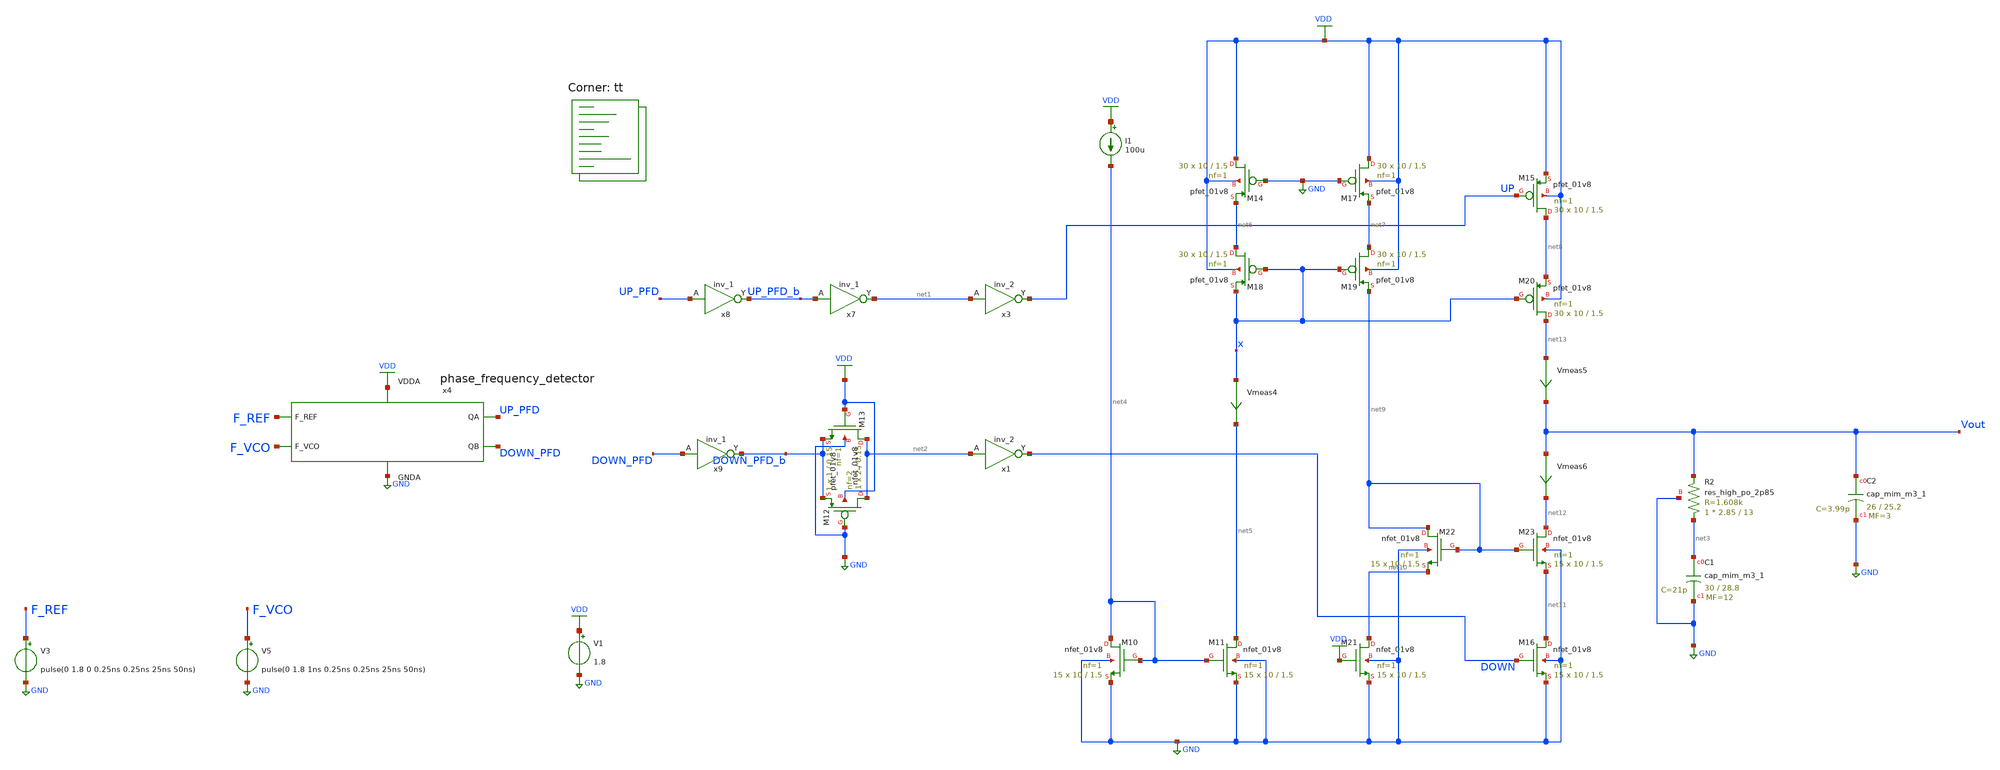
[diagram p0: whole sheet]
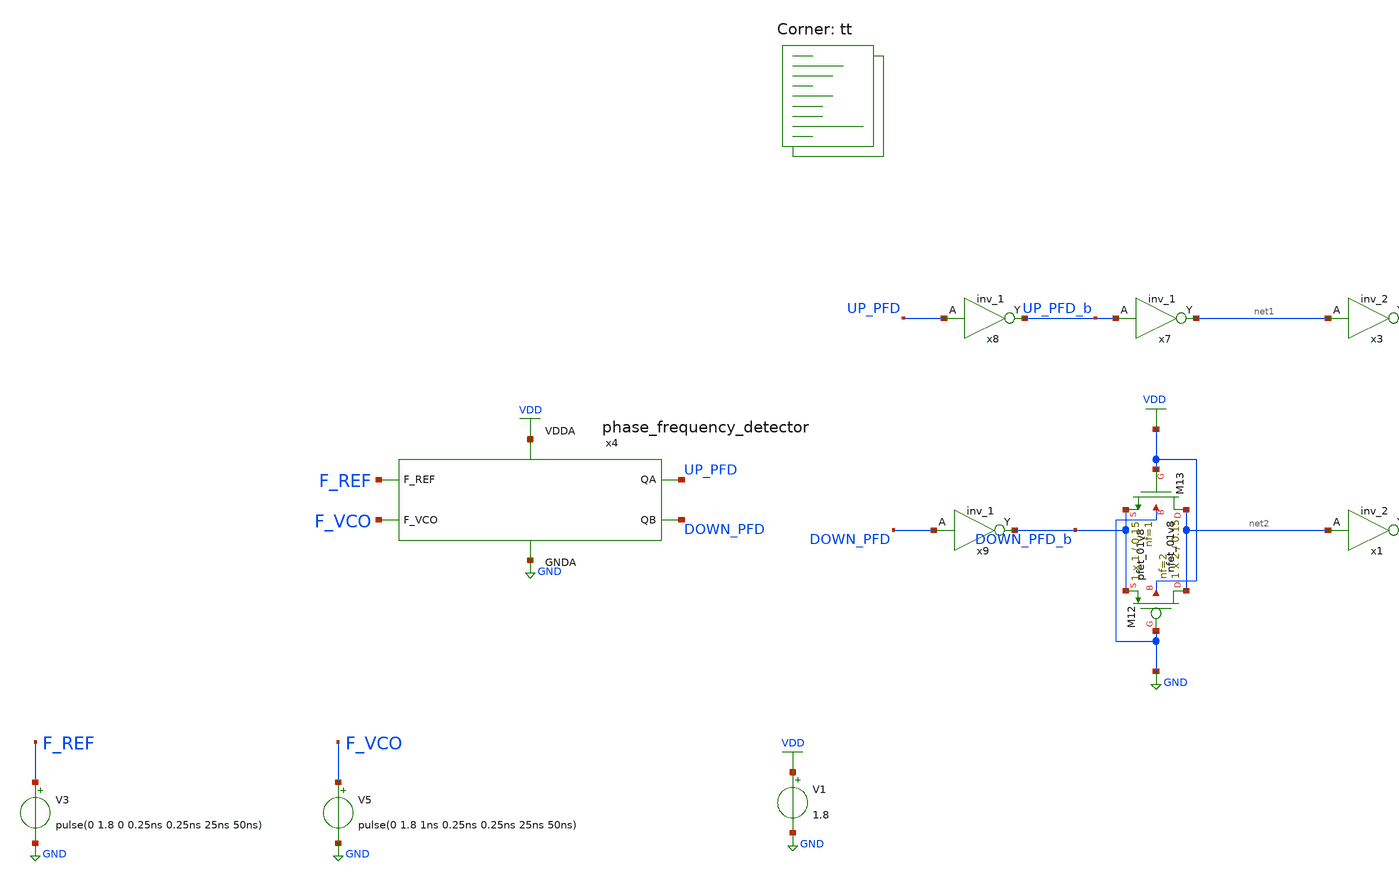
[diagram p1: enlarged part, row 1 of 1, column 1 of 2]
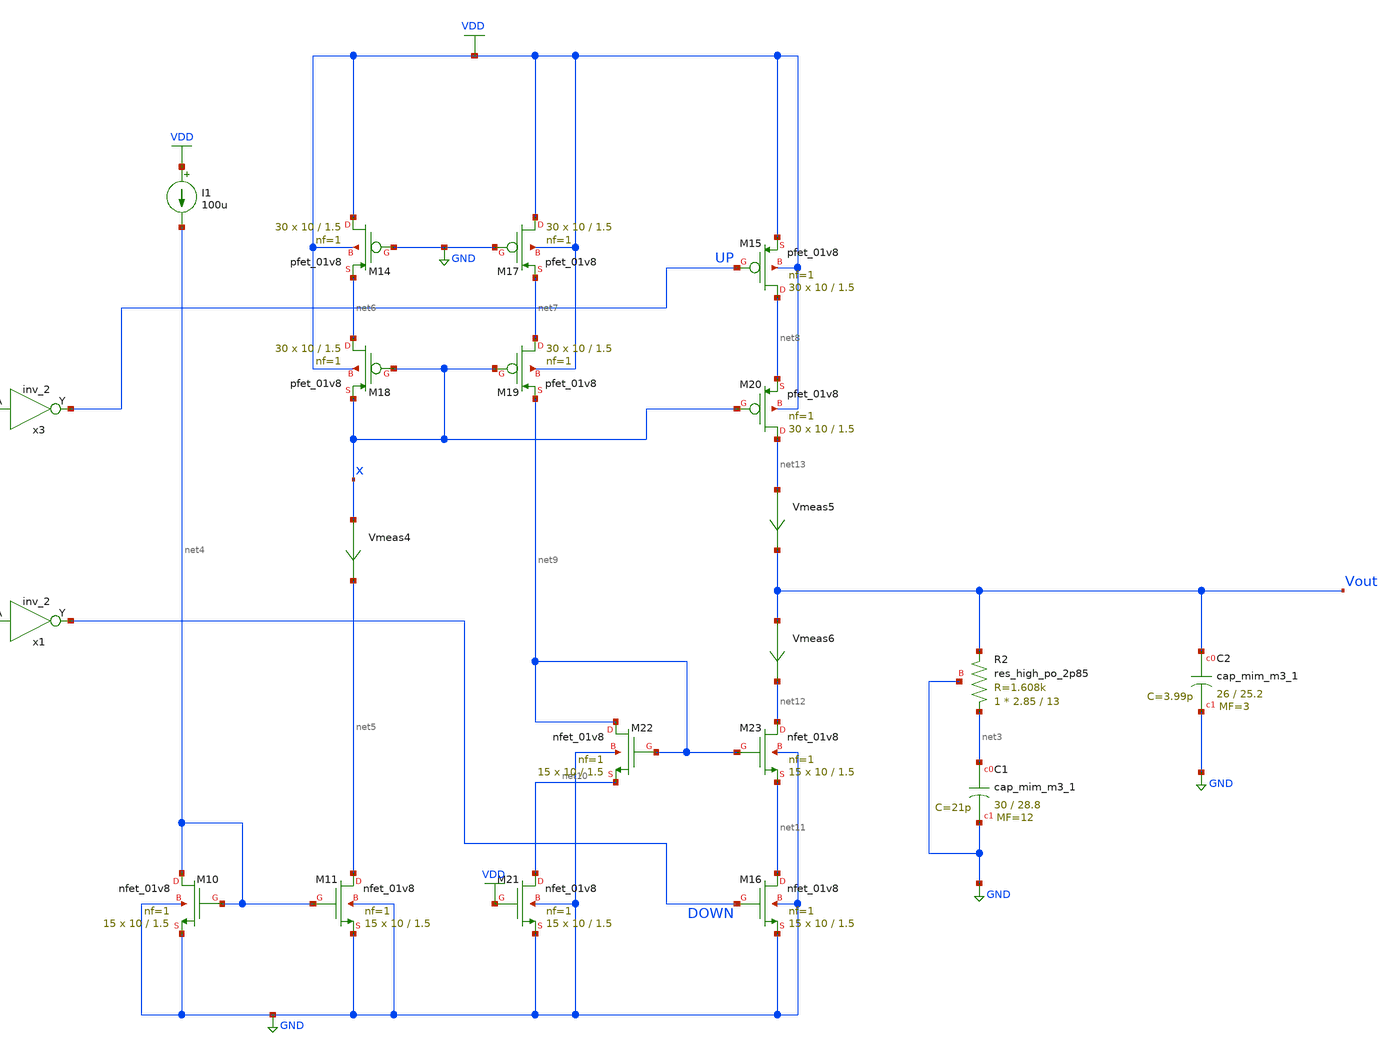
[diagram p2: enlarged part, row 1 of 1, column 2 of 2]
** sch_path: projects/pll/charge_pump/xschem_ngspice/pfd_charge_pump_2.sch
**.subckt pfd_charge_pump_2
V1 VDD GND 1.8
XM12 net2 GND DOWN_PFD_b VDD sky130_fd_pr__pfet_01v8 L=0.15 W=2 nf=2 ad='int((nf+1)/2) * W/nf * 0.29'
+ as='int((nf+2)/2) * W/nf * 0.29' pd='2*int((nf+1)/2) * (W/nf + 0.29)' ps='2*int((nf+2)/2) * (W/nf + 0.29)'
+ nrd='0.29 / W' nrs='0.29 / W' sa=0 sb=0 sd=0 mult=1 m=1
XM13 net2 VDD DOWN_PFD_b GND sky130_fd_pr__nfet_01v8 L=0.15 W=1 nf=1 ad='int((nf+1)/2) * W/nf * 0.29'
+ as='int((nf+2)/2) * W/nf * 0.29' pd='2*int((nf+1)/2) * (W/nf + 0.29)' ps='2*int((nf+2)/2) * (W/nf + 0.29)'
+ nrd='0.29 / W' nrs='0.29 / W' sa=0 sb=0 sd=0 mult=1 m=1
x7 UP_PFD_b GND GND VDD VDD net1 sky130_fd_sc_hd__inv_1
x8 UP_PFD GND GND VDD VDD UP_PFD_b sky130_fd_sc_hd__inv_1
x9 DOWN_PFD GND GND VDD VDD DOWN_PFD_b sky130_fd_sc_hd__inv_1
x3 net1 GND GND VDD VDD UP sky130_fd_sc_hd__inv_2
x1 net2 GND GND VDD VDD DOWN sky130_fd_sc_hd__inv_2
XC1 net3 GND sky130_fd_pr__cap_mim_m3_1 W=30 L=28.8 MF=12 m=12
XC2 Vout GND sky130_fd_pr__cap_mim_m3_1 W=26 L=25.2 MF=3 m=3
V3 F_REF GND pulse(0 1.8 0 0.25ns 0.25ns 25ns 50ns)
V5 F_VCO GND pulse(0 1.8 1ns 0.25ns 0.25ns 25ns 50ns)
x4 F_REF F_VCO VDD UP_PFD DOWN_PFD GND phase_frequency_detector
XM10 net4 net4 GND GND sky130_fd_pr__nfet_01v8 L=1.5 W=10 nf=1 ad='int((nf+1)/2) * W/nf * 0.29' as='int((nf+2)/2) * W/nf * 0.29'
+ pd='2*int((nf+1)/2) * (W/nf + 0.29)' ps='2*int((nf+2)/2) * (W/nf + 0.29)' nrd='0.29 / W' nrs='0.29 / W'
+ sa=0 sb=0 sd=0 mult=15 m=15
XM11 net5 net4 GND GND sky130_fd_pr__nfet_01v8 L=1.5 W=10 nf=1 ad='int((nf+1)/2) * W/nf * 0.29' as='int((nf+2)/2) * W/nf * 0.29'
+ pd='2*int((nf+1)/2) * (W/nf + 0.29)' ps='2*int((nf+2)/2) * (W/nf + 0.29)' nrd='0.29 / W' nrs='0.29 / W'
+ sa=0 sb=0 sd=0 mult=15 m=15
XM14 VDD GND net6 VDD sky130_fd_pr__pfet_01v8 L=1.5 W=10 nf=1 ad='int((nf+1)/2) * W/nf * 0.29' as='int((nf+2)/2) * W/nf * 0.29'
+ pd='2*int((nf+1)/2) * (W/nf + 0.29)' ps='2*int((nf+2)/2) * (W/nf + 0.29)' nrd='0.29 / W' nrs='0.29 / W'
+ sa=0 sb=0 sd=0 mult=30 m=30
I1 VDD net4 100u
Vmeas4 x net5 0
.save i(vmeas4)
XM15 net8 UP VDD VDD sky130_fd_pr__pfet_01v8 L=1.5 W=10 nf=1 ad='int((nf+1)/2) * W/nf * 0.29' as='int((nf+2)/2) * W/nf * 0.29'
+ pd='2*int((nf+1)/2) * (W/nf + 0.29)' ps='2*int((nf+2)/2) * (W/nf + 0.29)' nrd='0.29 / W' nrs='0.29 / W'
+ sa=0 sb=0 sd=0 mult=30 m=30
Vmeas5 net13 Vout 0
.save i(vmeas5)
Vmeas6 Vout net12 0
.save i(vmeas6)
XM16 net11 DOWN GND GND sky130_fd_pr__nfet_01v8 L=1.5 W=10 nf=1 ad='int((nf+1)/2) * W/nf * 0.29' as='int((nf+2)/2) * W/nf * 0.29'
+ pd='2*int((nf+1)/2) * (W/nf + 0.29)' ps='2*int((nf+2)/2) * (W/nf + 0.29)' nrd='0.29 / W' nrs='0.29 / W'
+ sa=0 sb=0 sd=0 mult=15 m=15
XM17 VDD GND net7 VDD sky130_fd_pr__pfet_01v8 L=1.5 W=10 nf=1 ad='int((nf+1)/2) * W/nf * 0.29' as='int((nf+2)/2) * W/nf * 0.29'
+ pd='2*int((nf+1)/2) * (W/nf + 0.29)' ps='2*int((nf+2)/2) * (W/nf + 0.29)' nrd='0.29 / W' nrs='0.29 / W'
+ sa=0 sb=0 sd=0 mult=30 m=30
XM18 net6 x x VDD sky130_fd_pr__pfet_01v8 L=1.5 W=10 nf=1 ad='int((nf+1)/2) * W/nf * 0.29' as='int((nf+2)/2) * W/nf * 0.29'
+ pd='2*int((nf+1)/2) * (W/nf + 0.29)' ps='2*int((nf+2)/2) * (W/nf + 0.29)' nrd='0.29 / W' nrs='0.29 / W'
+ sa=0 sb=0 sd=0 mult=30 m=30
XM19 net7 x net9 VDD sky130_fd_pr__pfet_01v8 L=1.5 W=10 nf=1 ad='int((nf+1)/2) * W/nf * 0.29' as='int((nf+2)/2) * W/nf * 0.29'
+ pd='2*int((nf+1)/2) * (W/nf + 0.29)' ps='2*int((nf+2)/2) * (W/nf + 0.29)' nrd='0.29 / W' nrs='0.29 / W'
+ sa=0 sb=0 sd=0 mult=30 m=30
XM20 net13 x net8 VDD sky130_fd_pr__pfet_01v8 L=1.5 W=10 nf=1 ad='int((nf+1)/2) * W/nf * 0.29' as='int((nf+2)/2) * W/nf * 0.29'
+ pd='2*int((nf+1)/2) * (W/nf + 0.29)' ps='2*int((nf+2)/2) * (W/nf + 0.29)' nrd='0.29 / W' nrs='0.29 / W'
+ sa=0 sb=0 sd=0 mult=30 m=30
XM21 net10 VDD GND GND sky130_fd_pr__nfet_01v8 L=1.5 W=10 nf=1 ad='int((nf+1)/2) * W/nf * 0.29' as='int((nf+2)/2) * W/nf * 0.29'
+ pd='2*int((nf+1)/2) * (W/nf + 0.29)' ps='2*int((nf+2)/2) * (W/nf + 0.29)' nrd='0.29 / W' nrs='0.29 / W'
+ sa=0 sb=0 sd=0 mult=15 m=15
XM22 net9 net9 net10 GND sky130_fd_pr__nfet_01v8 L=1.5 W=10 nf=1 ad='int((nf+1)/2) * W/nf * 0.29' as='int((nf+2)/2) * W/nf * 0.29'
+ pd='2*int((nf+1)/2) * (W/nf + 0.29)' ps='2*int((nf+2)/2) * (W/nf + 0.29)' nrd='0.29 / W' nrs='0.29 / W'
+ sa=0 sb=0 sd=0 mult=15 m=15
XM23 net12 net9 net11 GND sky130_fd_pr__nfet_01v8 L=1.5 W=10 nf=1 ad='int((nf+1)/2) * W/nf * 0.29' as='int((nf+2)/2) * W/nf * 0.29'
+ pd='2*int((nf+1)/2) * (W/nf + 0.29)' ps='2*int((nf+2)/2) * (W/nf + 0.29)' nrd='0.29 / W' nrs='0.29 / W'
+ sa=0 sb=0 sd=0 mult=15 m=15
XR2 net3 Vout GND sky130_fd_pr__res_high_po_2p85 L=13 mult=1 m=1
**** begin user architecture code
.lib $::SKYWATER_MODELS/sky130.lib.spice tt



.include /foss/pdks/sky130A/libs.ref/sky130_fd_sc_hd/spice/sky130_fd_sc_hd.spice

.option method=gear trtol1
.option wnflag=1
*.option savecurrents

* .ic v(osc)=0
* .temp = 75

.save  v(up_pfd) v(down_pfd) v(up_pfd_b) v(down_pfd_b) v(up) v(up_b) v(down) v(down_b) v(x) v(vout) v(up_input) v(down_input) v(f_ref) v(f_vco) v(x4.qa) v(x4.qa_b) v(x4.qb) v(x4.qb_b) v(x4.qa) v(x4.e) v(x4.e_b) v(x4.f) v(x4.f_b) v(x4.before_reset) v(x4.reset)


.control
  * save v(up_pfd) v(down_pfd) v(up_pfd_b) v(down_pfd_b) v(up) v(up_b) v(down) v(down_b) v(x)
+ v(vout) v(up_input) v(down_input)
  * save all
  tran 1ns 10us
  * dc V3 0 1.8 0.01 V3 0 1.8 1.8
  remzerovec
  write pfd_charge_pump_2.raw
  * wrdata /foss/designs/my_design/projects/pll/pfd/xschem_ngspice/charge_pump2_QA.txt v(osc)
  set appendwrite

.endc






**** end user architecture code
**.ends

* expanding   symbol:
*+  /foss/designs/my_design/projects/pll/pfd/xschem_ngspice/phase_frequency_detector.sym # of pins=6
** sym_path: projects/pll/pfd/xschem_ngspice/phase_frequency_detector.sym
** sch_path: projects/pll/pfd/xschem_ngspice/phase_frequency_detector.sch
.subckt phase_frequency_detector F_REF F_VCO VDDA QA QB GNDA
*.ipin F_REF
*.opin QA
*.ipin F_VCO
*.opin QB
*.ipin VDDA
*.ipin GNDA
x1 F_REF QA GNDA GNDA VDDA VDDA QA_b sky130_fd_sc_hd__nor2_1
x2 QA_b E GNDA GNDA VDDA VDDA QA sky130_fd_sc_hd__nor2_1
x3 QA_b E_b GNDA GNDA VDDA VDDA E sky130_fd_sc_hd__nor2_1
x4 E Reset GNDA GNDA VDDA VDDA E_b sky130_fd_sc_hd__nor2_1
x5 F_VCO QB GNDA GNDA VDDA VDDA QB_b sky130_fd_sc_hd__nor2_1
x6 QB_b F GNDA GNDA VDDA VDDA QB sky130_fd_sc_hd__nor2_1
x7 QB_b F_b GNDA GNDA VDDA VDDA F sky130_fd_sc_hd__nor2_1
x8 F Reset GNDA GNDA VDDA VDDA F_b sky130_fd_sc_hd__nor2_1
x9 QA QB GNDA GNDA VDDA VDDA before_Reset sky130_fd_sc_hd__nand2_1
x10 before_Reset GNDA GNDA VDDA VDDA net1 sky130_fd_sc_hd__inv_1
x11 net1 GNDA GNDA VDDA VDDA net2 sky130_fd_sc_hd__inv_1
x12 net2 GNDA GNDA VDDA VDDA net3 sky130_fd_sc_hd__inv_1
x13 net3 GNDA GNDA VDDA VDDA net4 sky130_fd_sc_hd__inv_1
x14 net4 GNDA GNDA VDDA VDDA Reset sky130_fd_sc_hd__inv_1
.ends

.GLOBAL GND
.GLOBAL VDD
.end
